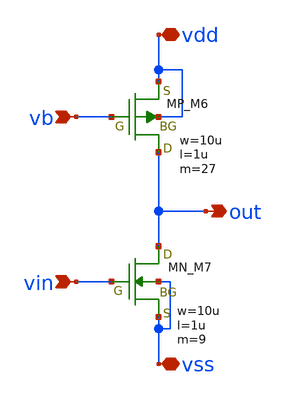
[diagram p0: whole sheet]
** sch_path: member_project/opamp/kubotakeshi/回路図/cs.sch
**.subckt cs vb vin out vss vdd
*.ipin vb
*.ipin vin
*.opin out
*.iopin vss
*.iopin vdd
XM6 out vb vdd vdd PMOS w=10u l=1u as=0 ad=0 ps=0 pd=0 nrd=0 nrs=0 m=27
XM7 out vin vss vss NMOS w=10u l=1u as=0 ad=0 ps=0 pd=0 nrd=0 nrs=0 m=9
**.ends
.end
